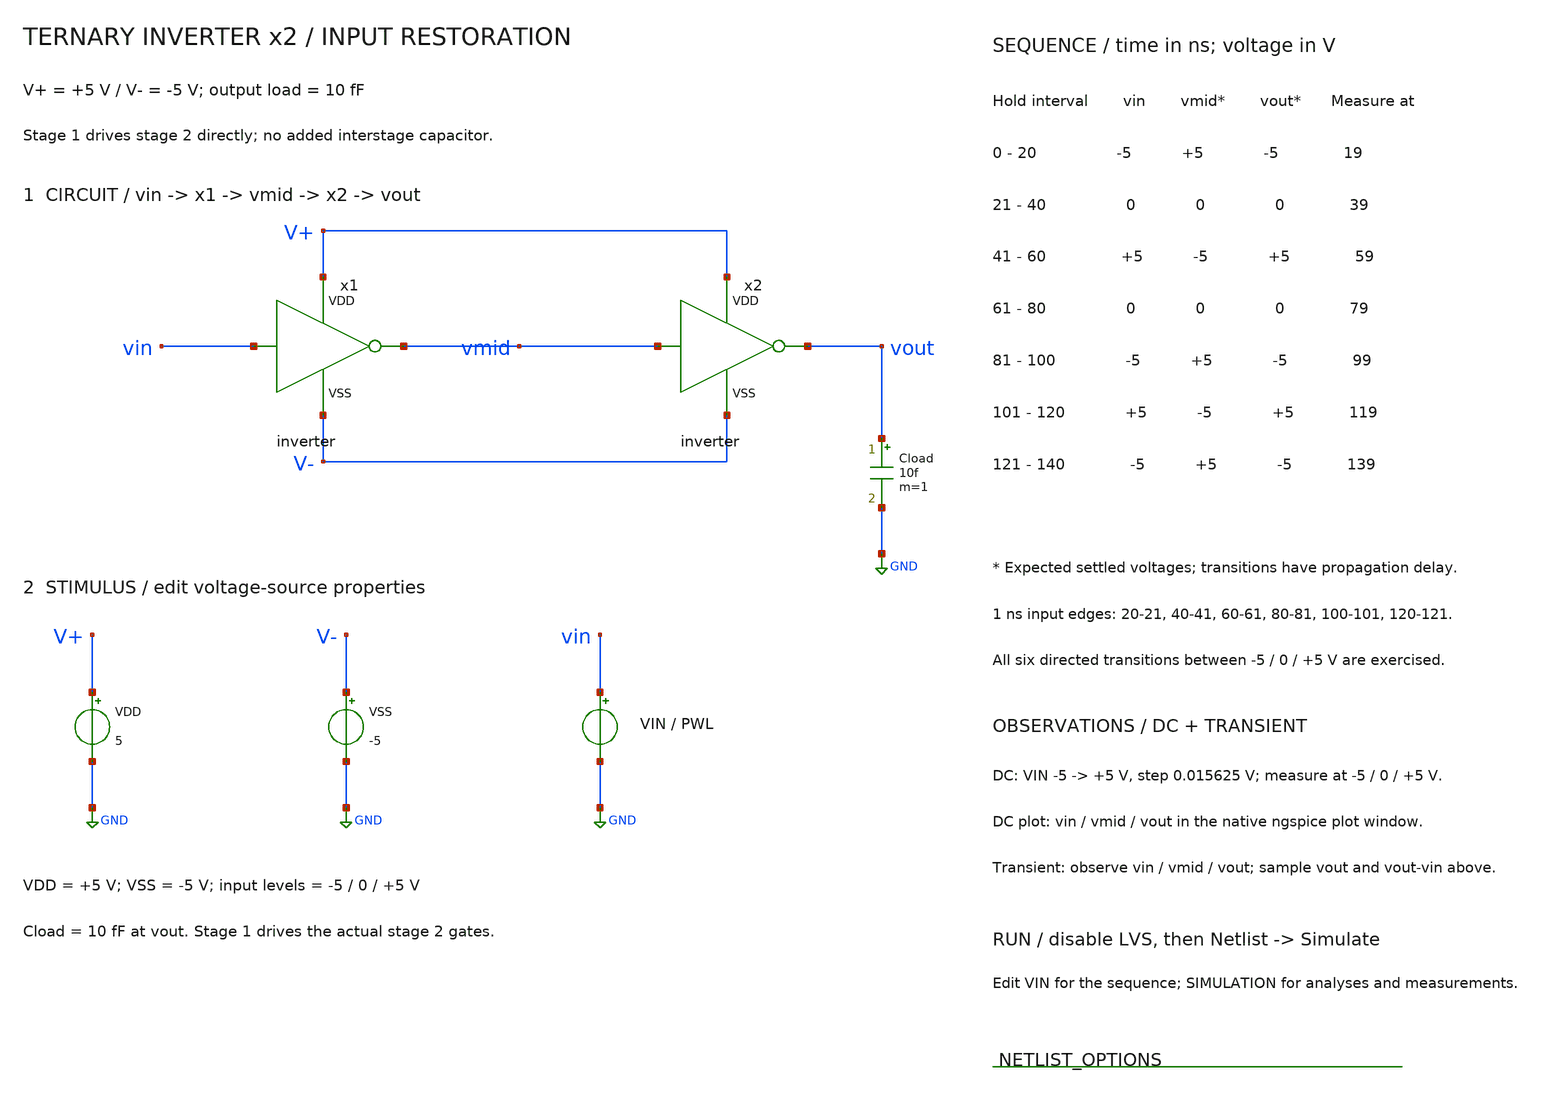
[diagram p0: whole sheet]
** sch_path: member_project/balanced-ternary-logic/PenguinEino/inverter_chain_tb.sch
**.subckt inverter_chain_tb
x1 vin vmid V+ V- inverter
x2 vmid vout V+ V- inverter
Cload vout GND 10f m=1
VDD V+ GND 5
VSS V- GND -5
VIN vin GND PWL(0 -5 20n -5 21n 0 40n 0 41n 5 60n 5 61n 0 80n 0 81n -5 100n -5 101n 5 120n 5 121n -5
+ 140n -5)
**** begin user architecture code
 .include $::LIB/ip62_models

.temp 27
.nodeset v(vmid)=5 v(vout)=-5
.control
save all
dc VIN -5 5 0.015625
let restore_error=v(vout)-v(vin)
meas dc OUT_NEG find v(vout) at=-5
meas dc OUT_ZERO find v(vout) at=0
meas dc OUT_POS find v(vout) at=5
plot v(vin) v(vmid) v(vout) ylimit -5.5 5.5 title 'DC transfer: two inverters'
reset
tran 0.05n 140n
let restore_error=v(vout)-v(vin)
meas tran OUT_NEG_1 find v(vout) at=19n
meas tran ERROR_NEG_1 find restore_error at=19n
meas tran OUT_ZERO_UP find v(vout) at=39n
meas tran ERROR_ZERO_UP find restore_error at=39n
meas tran OUT_POS_1 find v(vout) at=59n
meas tran ERROR_POS_1 find restore_error at=59n
meas tran OUT_ZERO_DOWN find v(vout) at=79n
meas tran ERROR_ZERO_DOWN find restore_error at=79n
meas tran OUT_NEG_2 find v(vout) at=99n
meas tran ERROR_NEG_2 find restore_error at=99n
meas tran OUT_POS_2 find v(vout) at=119n
meas tran ERROR_POS_2 find restore_error at=119n
meas tran OUT_NEG_3 find v(vout) at=139n
meas tran ERROR_NEG_3 find restore_error at=139n
plot v(vin) v(vmid) v(vout) ylimit -5.5 5.5 title 'Two inverters: input, stage 1, output'
.endc

**** end user architecture code
**.ends

* expanding   symbol:  /home/ishi-kai/balanced-ternary-logic/inverter.sym # of pins=4
** sym_path: member_project/balanced-ternary-logic/PenguinEino/inverter.sym
** sch_path: member_project/balanced-ternary-logic/PenguinEino/inverter.sch
.subckt inverter vin vout VDD VSS
*.iopin VDD
*.ipin vin
*.opin vout
*.iopin VSS
XXM1 net1 vin VDD VDD PMOS w=13.5u l=1u nrd=0 nrs=0 m=1
XR1 net1 vout VDD F_RR w=2.8e-06 l=30e-06 R=1 tc1=0 tc2=0 m=1
XR2 vout net2 VDD F_RR w=2.8e-06 l=30e-06 R=1 tc1=0 tc2=0 m=1
XXM2 net2 vin VSS VSS NMOS w=5u l=1u nrd=0 nrs=0 m=1
.ends

.GLOBAL GND
.end
